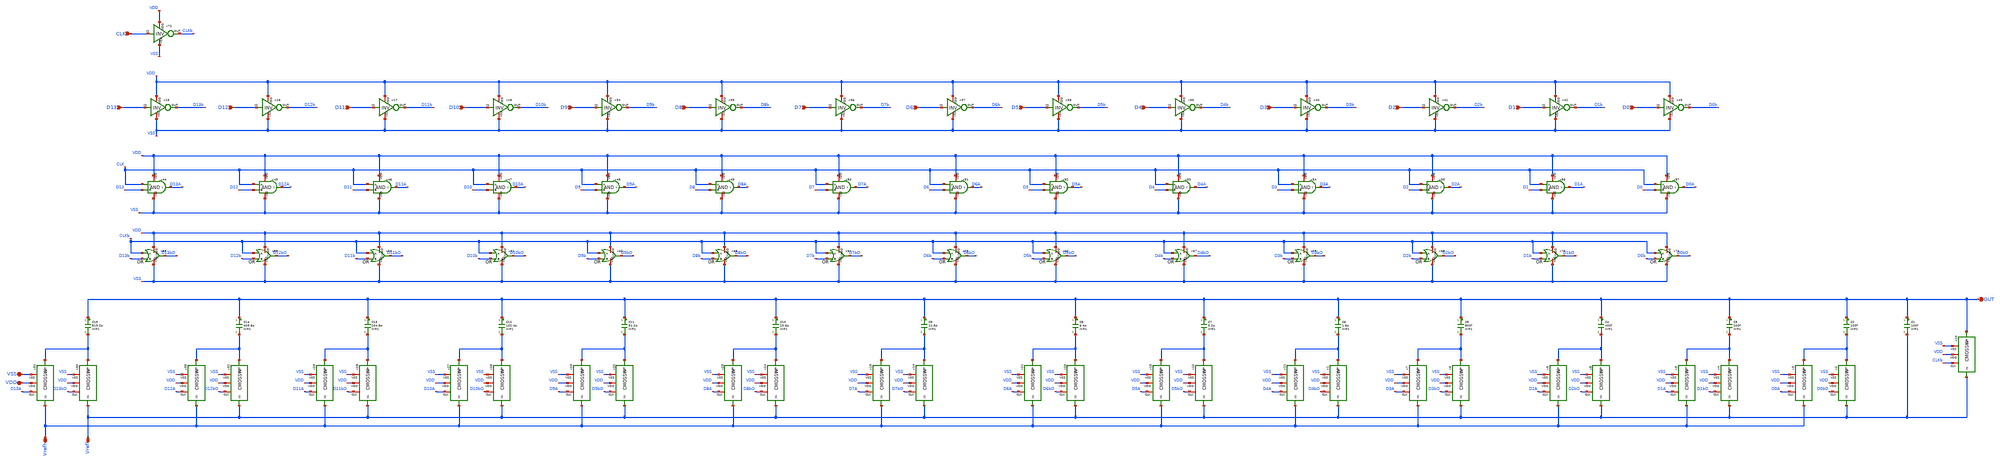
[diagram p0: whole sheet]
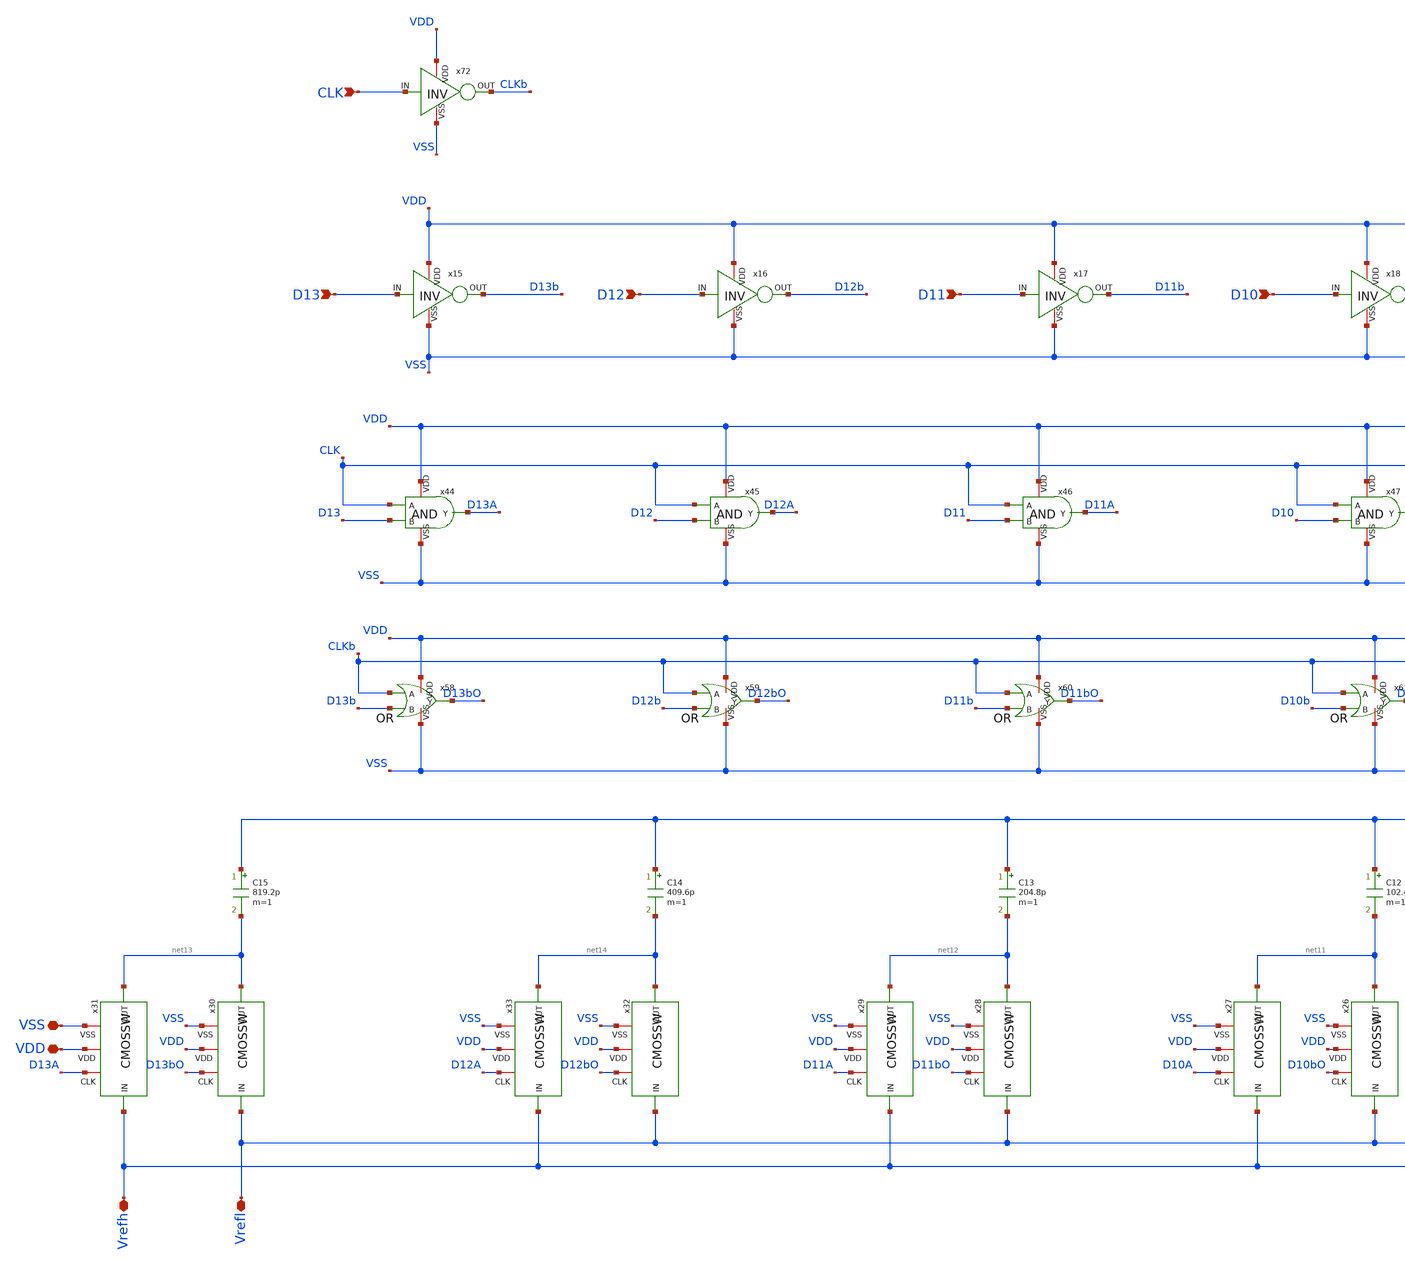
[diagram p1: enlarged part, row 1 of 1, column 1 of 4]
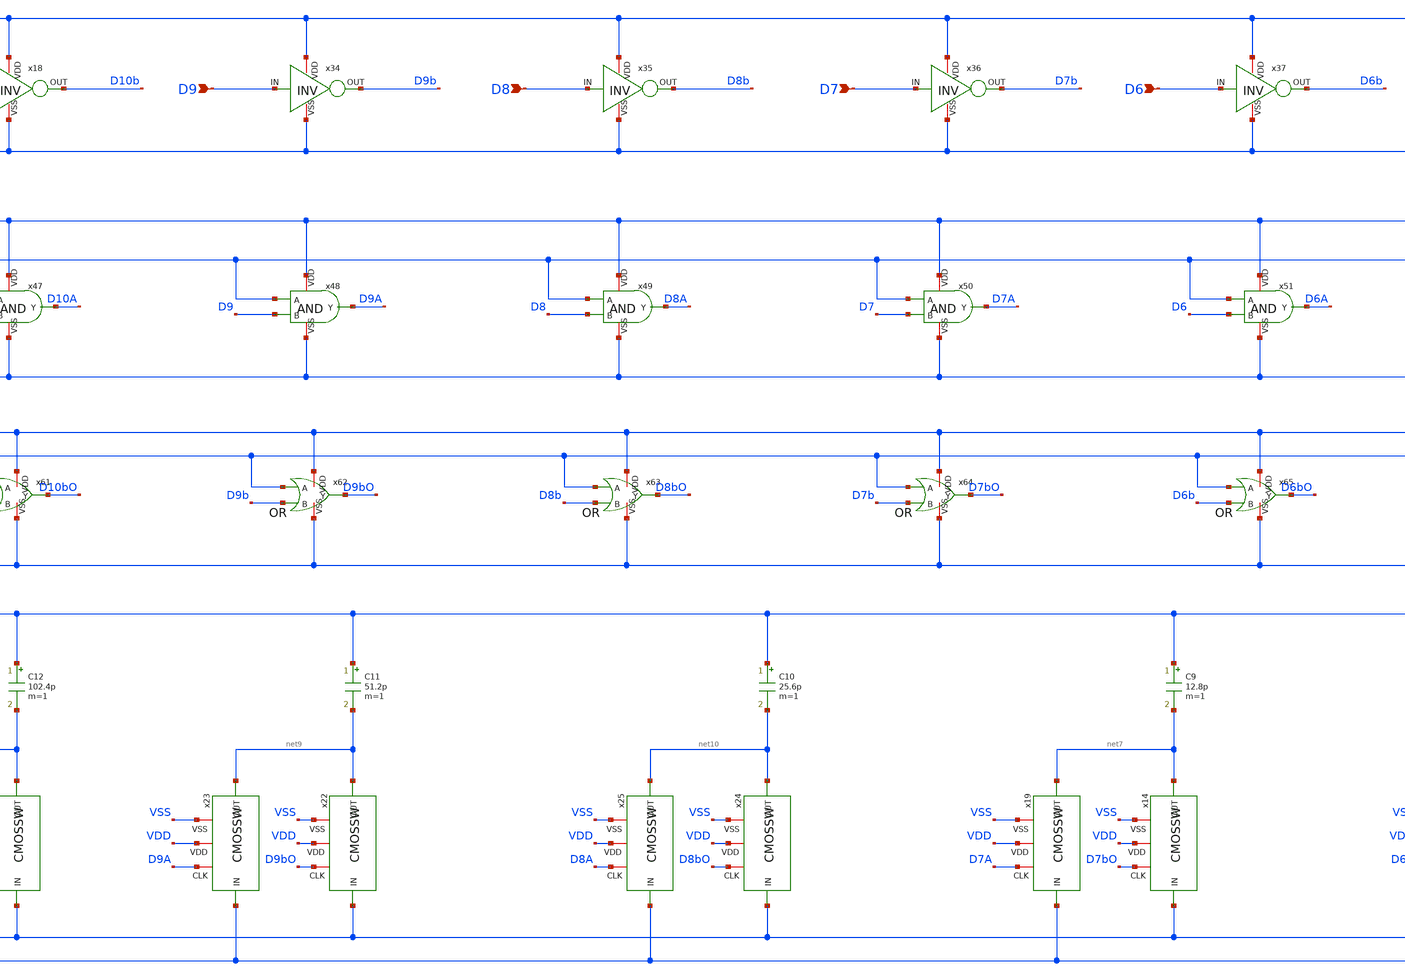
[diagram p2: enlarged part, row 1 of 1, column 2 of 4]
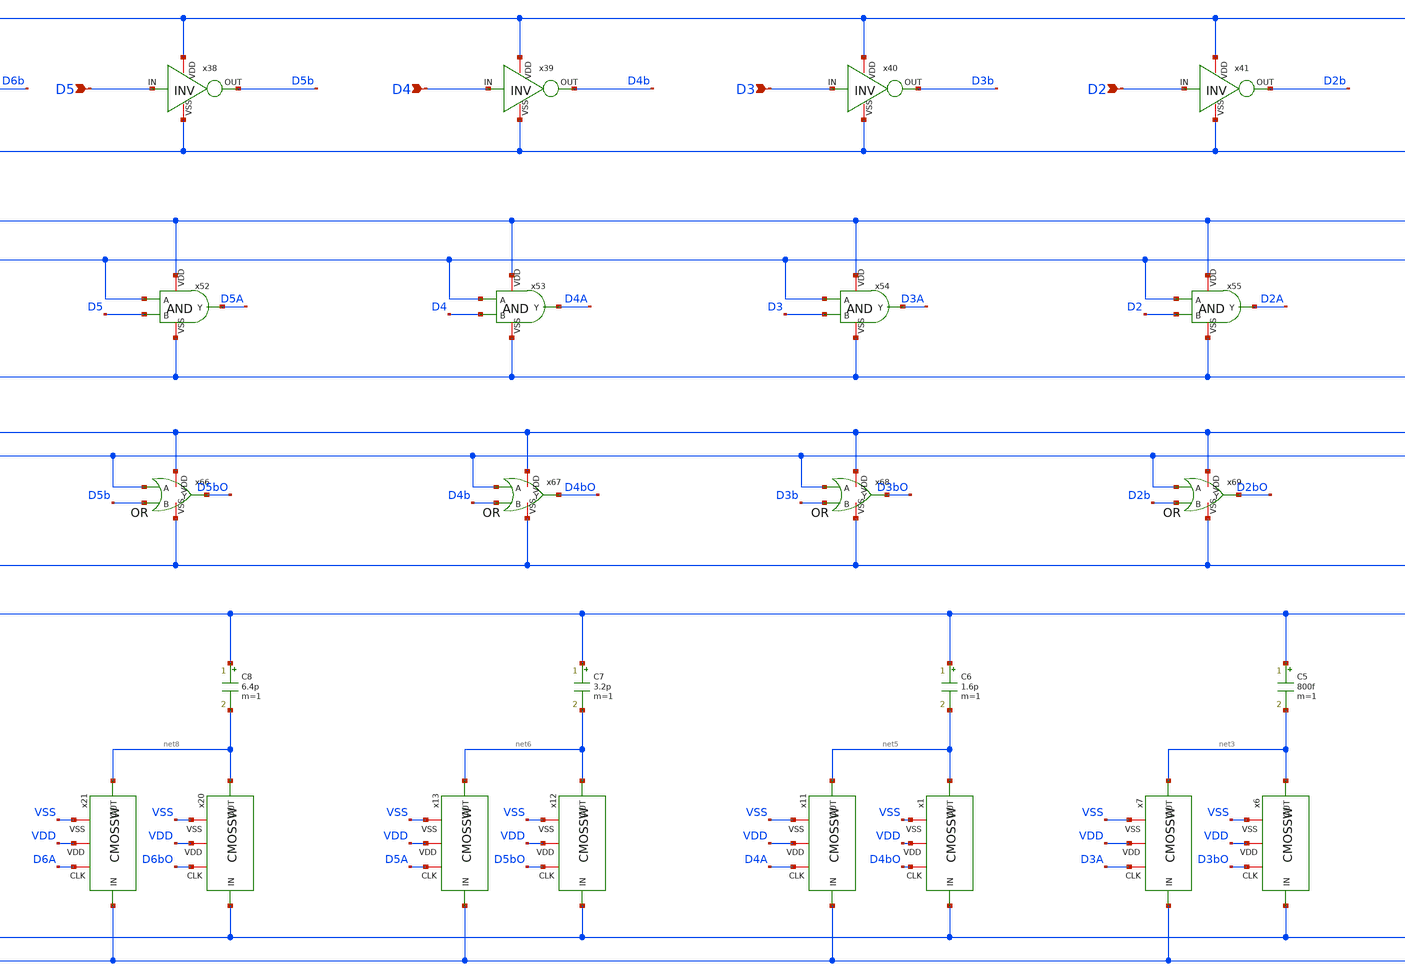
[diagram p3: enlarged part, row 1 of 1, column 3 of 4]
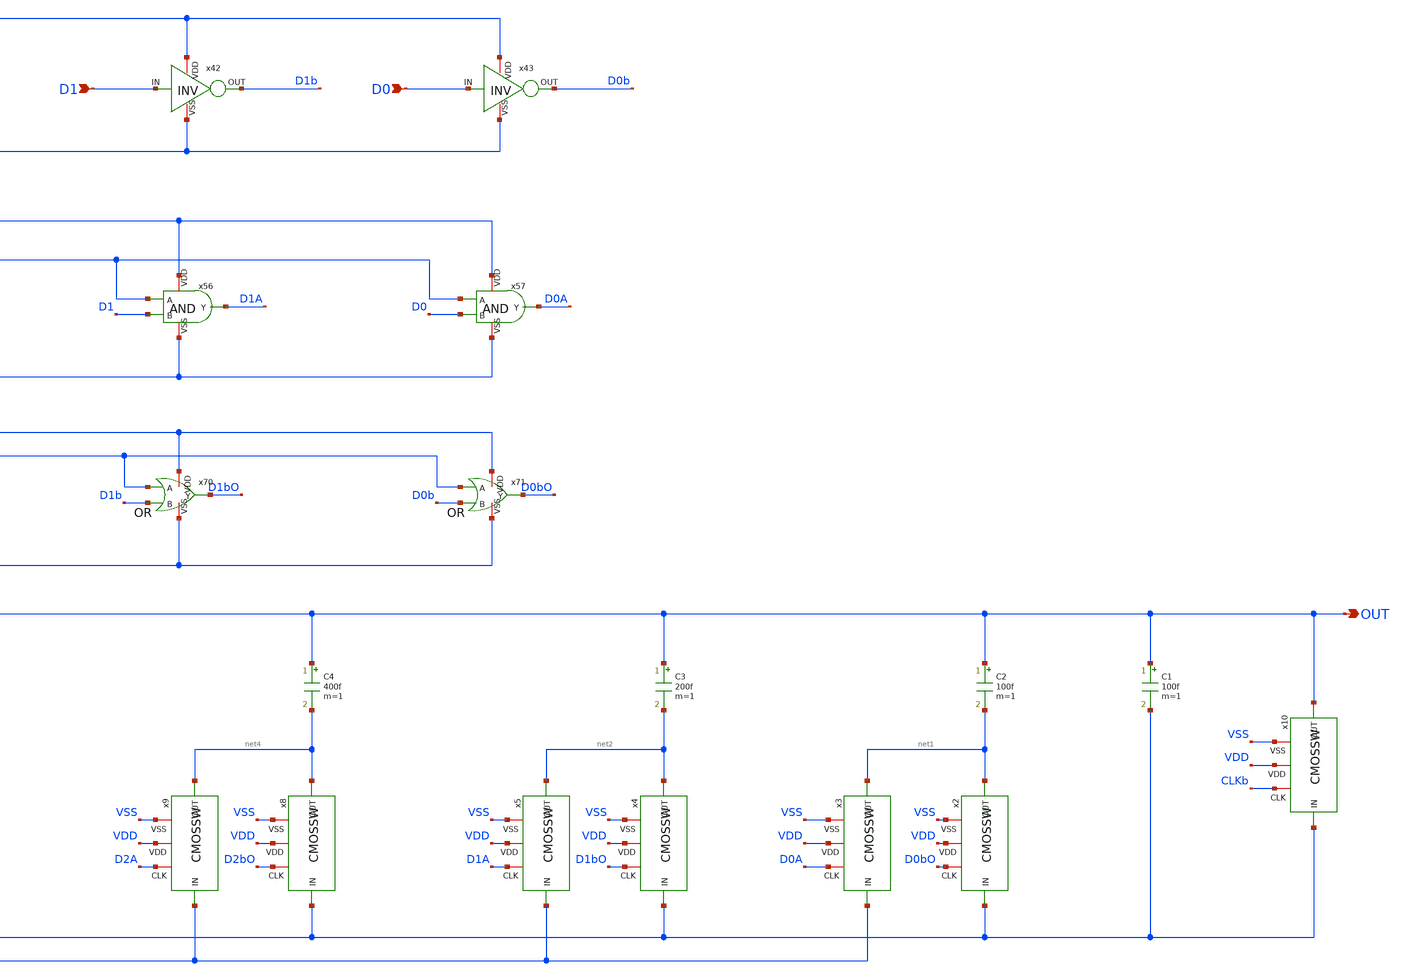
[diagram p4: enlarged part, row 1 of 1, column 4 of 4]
** sch_path: CDAC.sch
**.subckt CDAC OUT Vrefh Vrefl D13 D12 D11 D10 VSS VDD D9 D8 D7 D6 D5 D4 D3 D2 D1 D0 CLK
*.opin OUT
*.iopin Vrefh
*.iopin Vrefl
*.ipin D13
*.ipin D12
*.ipin D11
*.ipin D10
*.iopin VSS
*.iopin VDD
*.ipin D9
*.ipin D8
*.ipin D7
*.ipin D6
*.ipin D5
*.ipin D4
*.ipin D3
*.ipin D2
*.ipin D1
*.ipin D0
*.ipin CLK
C1 OUT Vrefl 100f m=1
C2 OUT net1 100f m=1
C3 OUT net2 200f m=1
C4 OUT net4 400f m=1
C5 OUT net3 800f m=1
x2 D0bO VSS net1 Vrefl VDD CMOSSW
x3 D0A VSS net1 Vrefh VDD CMOSSW
x4 D1bO VSS net2 Vrefl VDD CMOSSW
x5 D1A VSS net2 Vrefh VDD CMOSSW
x6 D3bO VSS net3 Vrefl VDD CMOSSW
x7 D3A VSS net3 Vrefh VDD CMOSSW
x8 D2bO VSS net4 Vrefl VDD CMOSSW
x10 CLKb VSS OUT Vrefl VDD CMOSSW
x9 D2A VSS net4 Vrefh VDD CMOSSW
x15 VDD D13b D13 VSS INV
x16 VDD D12b D12 VSS INV
x17 VDD D11b D11 VSS INV
x18 VDD D10b D10 VSS INV
C6 OUT net5 1.6p m=1
C7 OUT net6 3.2p m=1
C8 OUT net8 6.4p m=1
C9 OUT net7 12.8p m=1
x1 D4bO VSS net5 Vrefl VDD CMOSSW
x11 D4A VSS net5 Vrefh VDD CMOSSW
x12 D5bO VSS net6 Vrefl VDD CMOSSW
x13 D5A VSS net6 Vrefh VDD CMOSSW
x14 D7bO VSS net7 Vrefl VDD CMOSSW
x19 D7A VSS net7 Vrefh VDD CMOSSW
x20 D6bO VSS net8 Vrefl VDD CMOSSW
x21 D6A VSS net8 Vrefh VDD CMOSSW
C10 OUT net10 25.6p m=1
C11 OUT net9 51.2p m=1
x22 D9bO VSS net9 Vrefl VDD CMOSSW
x23 D9A VSS net9 Vrefh VDD CMOSSW
x24 D8bO VSS net10 Vrefl VDD CMOSSW
x25 D8A VSS net10 Vrefh VDD CMOSSW
C12 OUT net11 102.4p m=1
C13 OUT net12 204.8p m=1
C14 OUT net14 409.6p m=1
C15 OUT net13 819.2p m=1
x26 D10bO VSS net11 Vrefl VDD CMOSSW
x27 D10A VSS net11 Vrefh VDD CMOSSW
x28 D11bO VSS net12 Vrefl VDD CMOSSW
x29 D11A VSS net12 Vrefh VDD CMOSSW
x30 D13bO VSS net13 Vrefl VDD CMOSSW
x31 D13A VSS net13 Vrefh VDD CMOSSW
x32 D12bO VSS net14 Vrefl VDD CMOSSW
x33 D12A VSS net14 Vrefh VDD CMOSSW
x34 VDD D9b D9 VSS INV
x35 VDD D8b D8 VSS INV
x36 VDD D7b D7 VSS INV
x37 VDD D6b D6 VSS INV
x38 VDD D5b D5 VSS INV
x39 VDD D4b D4 VSS INV
x40 VDD D3b D3 VSS INV
x41 VDD D2b D2 VSS INV
x42 VDD D1b D1 VSS INV
x43 VDD D0b D0 VSS INV
x44 VDD D13A CLK D13 VSS AND
x45 VDD D12A CLK D12 VSS AND
x46 VDD D11A CLK D11 VSS AND
x47 VDD D10A CLK D10 VSS AND
x48 VDD D9A CLK D9 VSS AND
x49 VDD D8A CLK D8 VSS AND
x50 VDD D7A CLK D7 VSS AND
x51 VDD D6A CLK D6 VSS AND
x52 VDD D5A CLK D5 VSS AND
x53 VDD D4A CLK D4 VSS AND
x54 VDD D3A CLK D3 VSS AND
x55 VDD D2A CLK D2 VSS AND
x56 VDD D1A CLK D1 VSS AND
x57 VDD D0A CLK D0 VSS AND
x58 VDD CLKb D13bO D13b VSS OR
x59 VDD CLKb D12bO D12b VSS OR
x60 VDD CLKb D11bO D11b VSS OR
x61 VDD CLKb D10bO D10b VSS OR
x62 VDD CLKb D9bO D9b VSS OR
x63 VDD CLKb D8bO D8b VSS OR
x64 VDD CLKb D7bO D7b VSS OR
x65 VDD CLKb D6bO D6b VSS OR
x66 VDD CLKb D5bO D5b VSS OR
x67 VDD CLKb D4bO D4b VSS OR
x68 VDD CLKb D3bO D3b VSS OR
x69 VDD CLKb D2bO D2b VSS OR
x70 VDD CLKb D1bO D1b VSS OR
x71 VDD CLKb D0bO D0b VSS OR
x72 VDD CLKb CLK VSS INV
**.ends

* expanding   symbol:  C:/Users/ISLab2/Documents/minimal_LR/CMOSSW.sym # of pins=5
** sym_path: CMOSSW.sym
** sch_path: CMOSSW.sch
.subckt CMOSSW CLK VSS OUT IN VDD
*.ipin IN
*.iopin VSS
*.opin OUT
*.iopin CLK
*.iopin VDD
M1 OUT CLK IN VSS nch w=10u l=0.35u as=0 ps=0 ad=0 pd=0 m=1
M5 OUT net1 IN VDD pch w=10u l=0.35u as=0 ps=0 ad=0 pd=0 m=1
x1 VDD net1 CLK VSS INV
.ends


* expanding   symbol:  C:/Users/ISLab2/Documents/minimal_LR/INV.sym # of pins=4
** sym_path: INV.sym
** sch_path: INV.sch
.subckt INV VDD OUT IN VSS
*.opin OUT
*.ipin IN
*.iopin VDD
*.iopin VSS
M2 OUT IN VDD VDD pch w=10u l=0.35u as=0 ps=0 ad=0 pd=0 m=1
M1 OUT IN VSS VSS nch w=5u l=0.35u as=0 ps=0 ad=0 pd=0 m=1
.ends


* expanding   symbol:  C:/Users/ISLab2/Documents/minimal_LR/AND.sym # of pins=5
** sym_path: AND.sym
** sch_path: AND.sch
.subckt AND VDD Y A B VSS
*.iopin VDD
*.ipin A
*.ipin B
*.iopin VSS
*.opin Y
M1 net1 A net2 VSS nch w=3.5u l=0.35u as=0 ps=0 ad=0 pd=0 m=1
M2 net1 B VDD VDD pch w=3.5u l=0.35u as=0 ps=0 ad=0 pd=0 m=1
M3 net1 A VDD VDD pch w=3.5u l=0.35u as=0 ps=0 ad=0 pd=0 m=1
M4 net2 B VSS VSS nch w=3.5u l=0.35u as=0 ps=0 ad=0 pd=0 m=1
M5 Y net1 VDD VDD pch w=3.5u l=0.35u as=0 ps=0 ad=0 pd=0 m=1
M6 Y net1 VSS VSS nch w=3.5u l=0.35u as=0 ps=0 ad=0 pd=0 m=1
**** begin user architecture code


.include C:/Users/ISLab2/Documents/minimal_LR/minimal.txt

**** end user architecture code
.ends


* expanding   symbol:  C:/Users/ISLab2/Documents/minimal_LR/OR.sym # of pins=5
** sym_path: OR.sym
** sch_path: OR.sch
.subckt OR VDD A Y B VSS
*.iopin VDD
*.ipin A
*.ipin B
*.iopin VSS
*.opin Y
M1 net1 A VSS VSS nch w=3.5u l=0.35u as=0 ps=0 ad=0 pd=0 m=1
M2 net2 A VDD VDD pch w=3.5u l=0.35u as=0 ps=0 ad=0 pd=0 m=1
M3 net1 B net2 VDD pch w=3.5u l=0.35u as=0 ps=0 ad=0 pd=0 m=1
M4 net1 B VSS VSS nch w=3.5u l=0.35u as=0 ps=0 ad=0 pd=0 m=1
M5 Y net1 VDD VDD pch w=3.5u l=0.35u as=0 ps=0 ad=0 pd=0 m=1
M6 Y net1 VSS VSS nch w=3.5u l=0.35u as=0 ps=0 ad=0 pd=0 m=1
**** begin user architecture code


.include C:/Users/ISLab2/Documents/minimal_LR/minimal.txt

**** end user architecture code
.ends

.end
